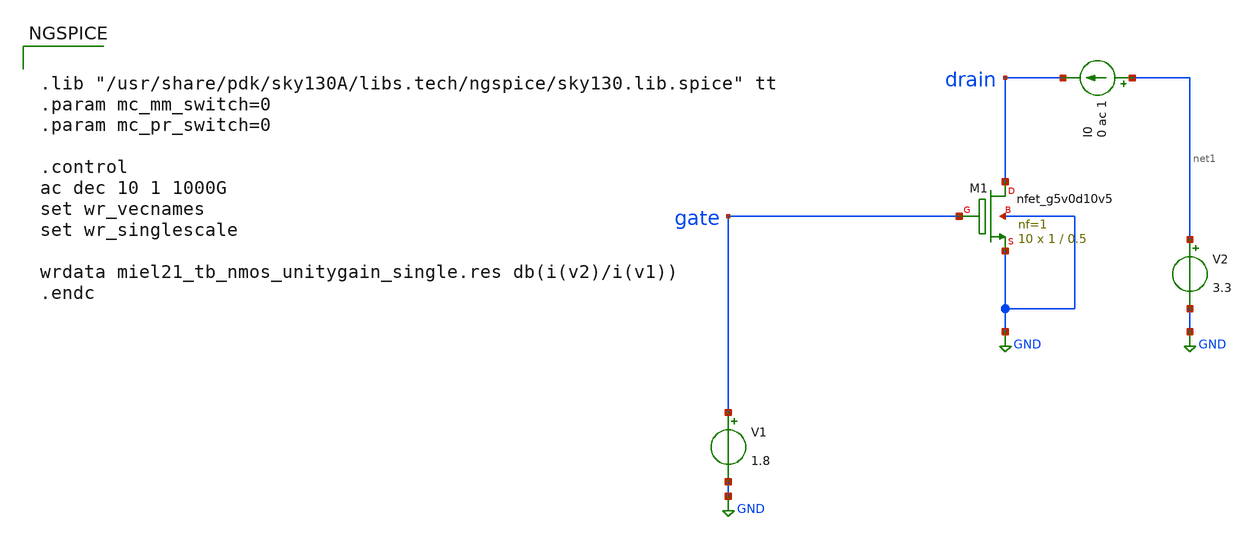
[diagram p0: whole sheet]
** sch_path: dev/opamp/miel21_tb_nmos_unitygain_single.sch
**.subckt miel21_tb_nmos_unitygain_single
V2 net1 GND 3.3
XM1 drain gate GND GND sky130_fd_pr__nfet_g5v0d10v5 L=0.5 W=1 nf=1 ad='int((nf+1)/2) * W/nf * 0.29' as='int((nf+2)/2) * W/nf * 0.29'
+ pd='2*int((nf+1)/2) * (W/nf + 0.29)' ps='2*int((nf+2)/2) * (W/nf + 0.29)' nrd='0.29 / W' nrs='0.29 / W'
+ sa=0 sb=0 sd=0 mult=10 m=10
V1 gate GND 1.8
I0 net1 drain 0 ac 1
**** begin user architecture code


.lib "/usr/share/pdk/sky130A/libs.tech/ngspice/sky130.lib.spice" tt
.param mc_mm_switch=0
.param mc_pr_switch=0

.control
ac dec 10 1 1000G
set wr_vecnames
set wr_singlescale

wrdata miel21_tb_nmos_unitygain_single.res db(i(v2)/i(v1))
.endc


**** end user architecture code
**.ends
.GLOBAL GND
.end
